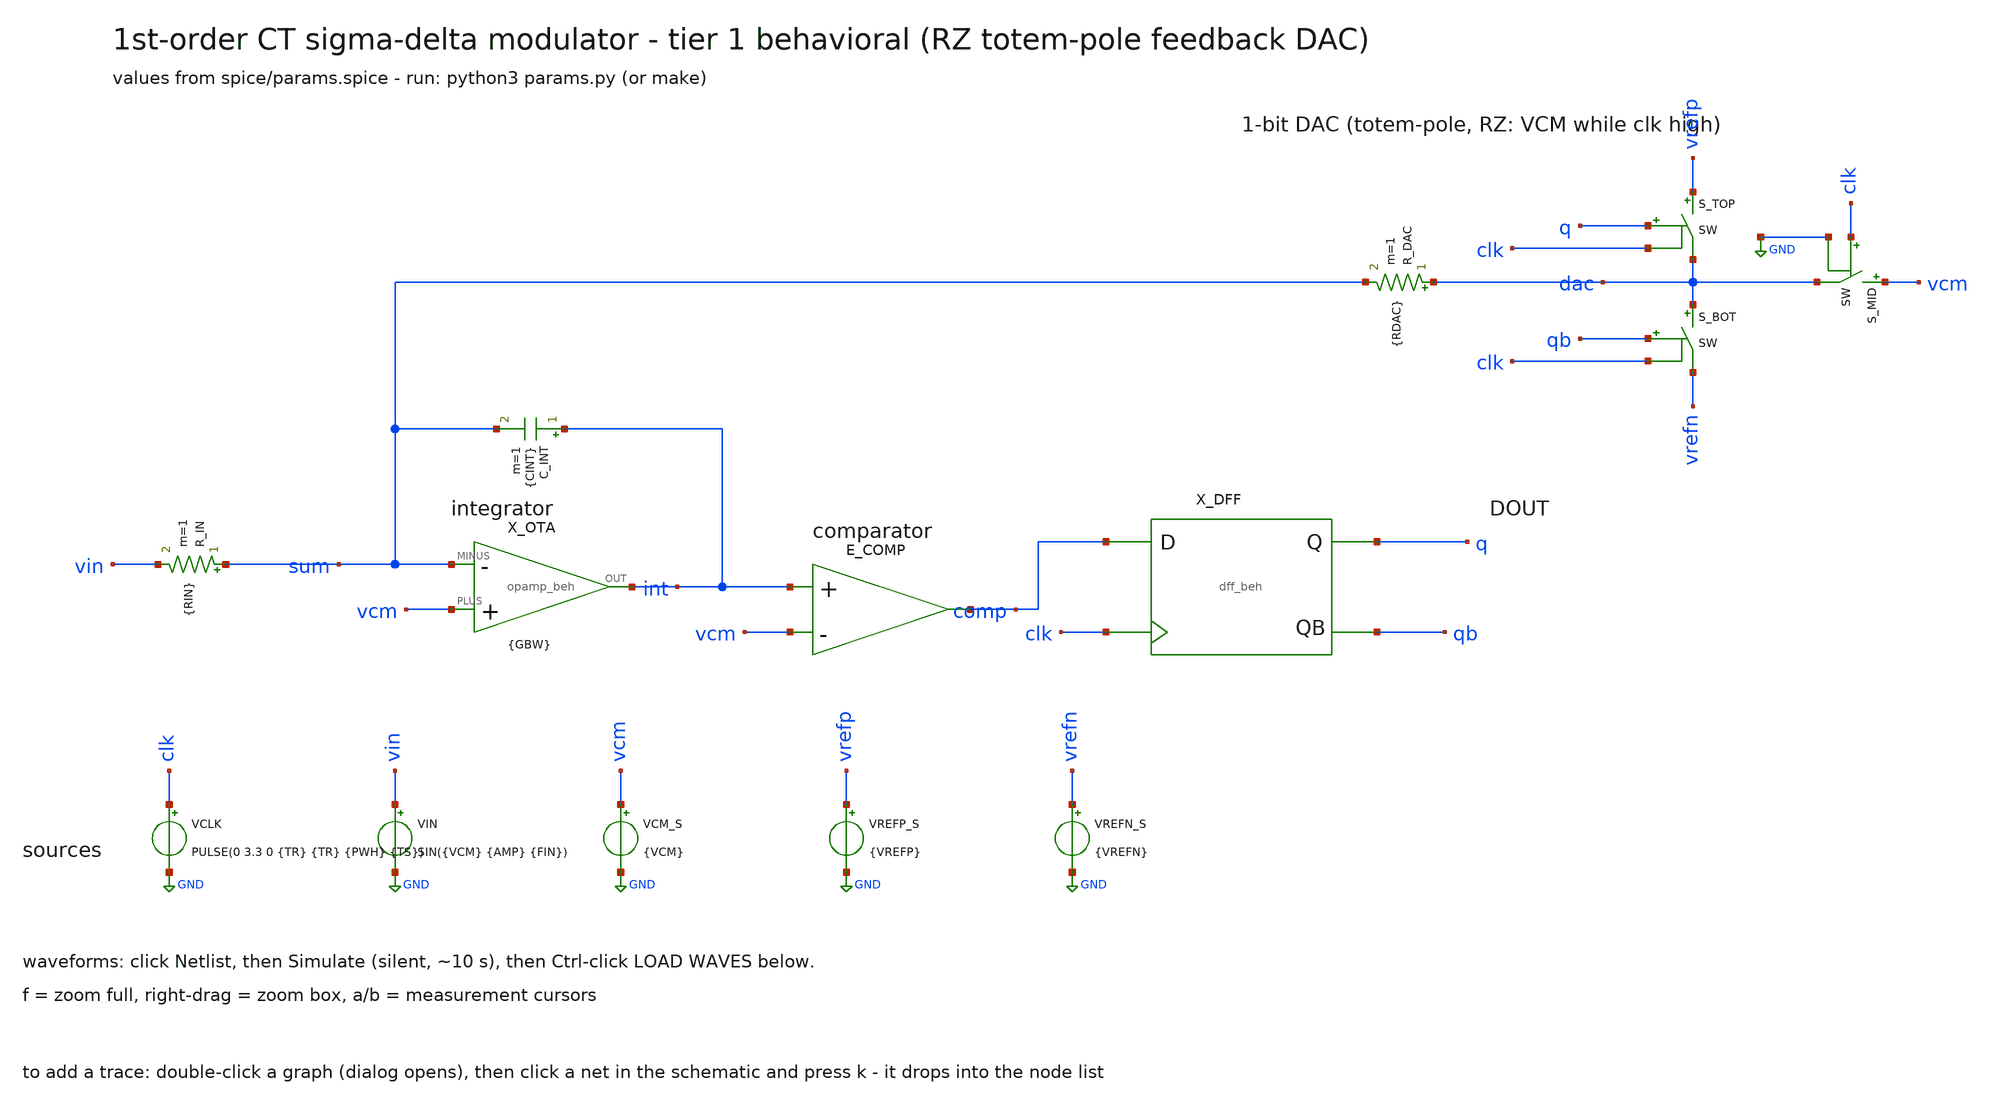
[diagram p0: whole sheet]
** sch_path: xschem/tier1_sdm.sch
**.subckt tier1_sdm
R_IN sum vin {RIN} m=1
X_OTA vcm sum int ota_beh AOL={AOL} GBW={GBW} SR={SR}
C_INT int sum {CINT} m=1
E_COMP comp GND VOL='1.65+1.65*tanh(2000*(v( int )-v( vcm )))'
X_DFF comp clk q qb dff_beh
S_TOP vrefp dac q clk SW
S_BOT dac vrefn qb clk SW
S_MID vcm dac clk GND SW
R_DAC dac sum {RDAC} m=1
VCLK clk GND PULSE(0 3.3 0 {TR} {TR} {PWH} {TS})
VIN vin GND SIN({VCM} {AMP} {FIN})
VCM_S vcm GND {VCM}
VREFP_S vrefp GND {VREFP}
VREFN_S vrefn GND {VREFN}
**** begin user architecture code

.include params.spice
.model SW sw vt=1.65 vh=0.1 ron=100 roff=1e9
* behavioral OTA: single-pole, slew-limited (AOL, GBW [Hz], SR [V/s])
.subckt ota_beh PLUS MINUS OUT AOL=10000 GBW=200e6 SR=2e8
.param CI=100f
.param GMI={6.2831853*GBW*CI}
.param ILIM={SR*CI}
.param RO={AOL/GMI}
B_GM 0 x I={ILIM}*tanh({GMI}*(v(PLUS)-v(MINUS))/{ILIM})
R_O x 0 {RO}
C_O x 0 {CI}
E_BUF OUT 0 x 0 1
.ends
* behavioral DFF: master/slave sample-and-hold of D at rising CLK edge
.subckt dff_beh D CLK Q QB
V_L vddl 0 3.3
S_M D m vddl CLK SW
C_M m 0 100f
S_S m qraw CLK 0 SW
C_Q qraw 0 100f
E_Q Q 0 VOL='1.65+1.65*tanh(20*(v(qraw)-1.65))'
E_QB QB 0 VOL='3.3-v(Q)'
.ends
.ic v(int)={VCM}
.tran {TSTEP} {TSTOP} uic
.control
run
write tier1_sdm.raw
wrdata tier1_out.csv v(q) v(clk) v(vin) v(int)
.endc


**** end user architecture code
**.ends
.GLOBAL GND
.end
